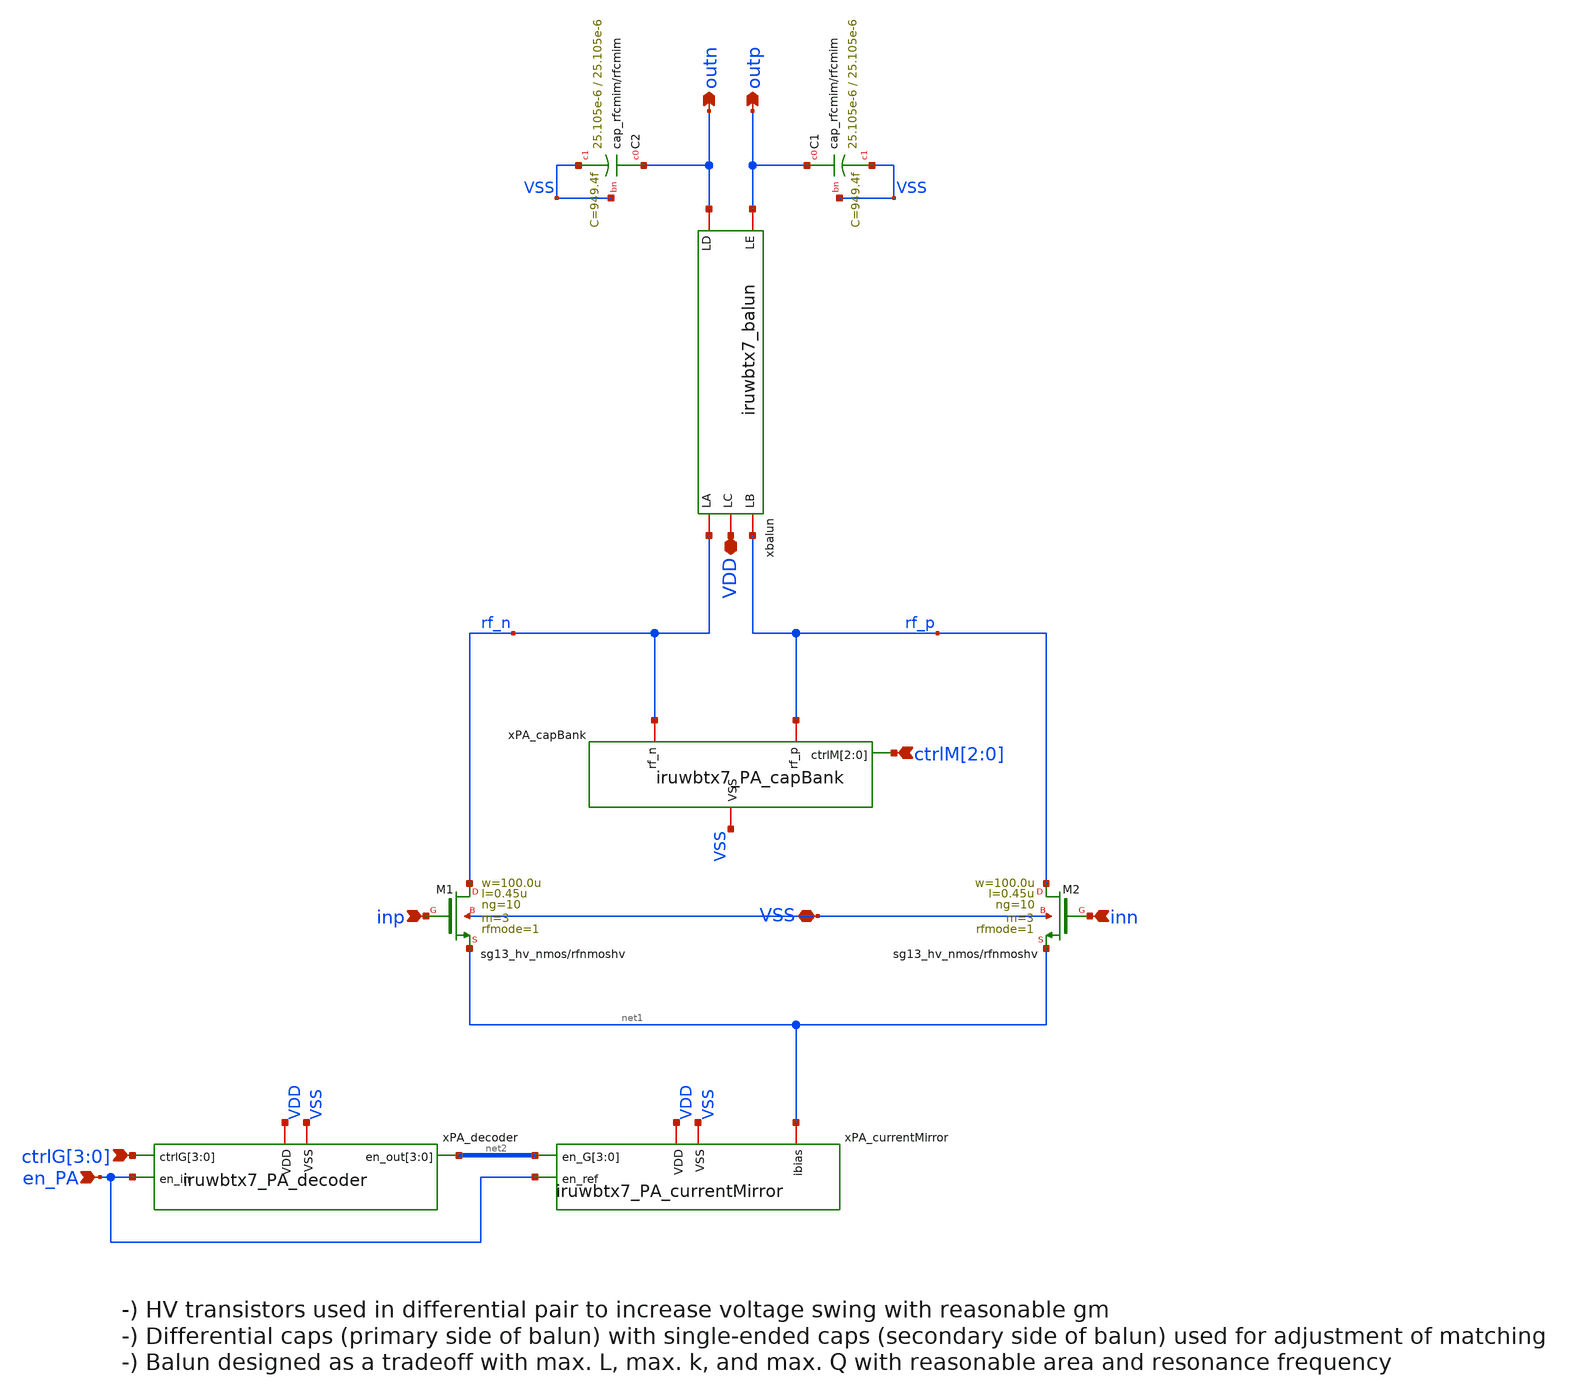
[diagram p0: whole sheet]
** sch_path: xschem/iruwbtx7_PA.sch
* IHP-GmbH/IHP-Open-PDK/ihp-sg13g2/libs.tech/xschem/sg13g2_stdcells/sg13g2_inv_16.sch:
* Copyright 2023 IHP PDK Authors
* Licensed under the Apache License, Version 2.0 (the "License");
**.subckt iruwbtx7_PA VDD outn outp ctrlM[2],ctrlM[1],ctrlM[0] inp inn VSS
*+ ctrlG[3],ctrlG[2],ctrlG[1],ctrlG[0] en_PA
*.iopin VDD
*.opin outn
*.opin outp
*.ipin ctrlM[2],ctrlM[1],ctrlM[0]
*.ipin inp
*.ipin inn
*.iopin VSS
*.ipin ctrlG[3],ctrlG[2],ctrlG[1],ctrlG[0]
*.ipin en_PA
xbalun outn outp VDD rf_p rf_n iruwbtx7_balun
XC2 outn VSS VSS cap_rfcmim w=25.105e-6 l=25.105e-6 wfeed=3.0e-6 m=1 mm_ok=1
XC1 outp VSS VSS cap_rfcmim w=25.105e-6 l=25.105e-6 wfeed=3.0e-6 m=1 mm_ok=1
xPA_capBank rf_n rf_p ctrlM[2] ctrlM[1] ctrlM[0] VSS iruwbtx7_PA_capBank
XM2 rf_p inn net1 VSS sg13_hv_nmos w=100.0u l=0.45u ng=10 m=3 rfmode=1 mm_ok=1
XM1 rf_n inp net1 VSS sg13_hv_nmos w=100.0u l=0.45u ng=10 m=3 rfmode=1 mm_ok=1
xPA_currentMirror VDD net2[3] net2[2] net2[1] net2[0] net1 en_PA VSS iruwbtx7_PA_currentMirror
xPA_decoder VDD VSS ctrlG[3] ctrlG[2] ctrlG[1] ctrlG[0] net2[3] net2[2] net2[1] net2[0] en_PA
+ iruwbtx7_PA_decoder
**.ends

* expanding   symbol:  iruwbtx7_balun.sym # of pins=5
** sym_path: xschem/iruwbtx7_balun.sym
** sch_path: xschem/iruwbtx7_balun.sch
.subckt iruwbtx7_balun LD LE LC LB LA
*.iopin LC
*.iopin LA
*.iopin LB
*.iopin LD
*.iopin LE
L1 LC net2 411p m=1
L2 net1 LC 411p m=1
R1 net2 LA 2.18 m=1
R2 LB net1 2.18 m=1
L3 net3 net5 483p m=1
L4 net4 net3 483p m=1
R3 net5 LD 3.6 m=1
R4 LE net4 3.6 m=1
K1 L1 L3 0.74
K2 L2 L4 0.74
.ends


* expanding   symbol:  iruwbtx7_PA_capBank.sym # of pins=4
** sym_path: xschem/iruwbtx7_PA_capBank.sym
** sch_path: xschem/iruwbtx7_PA_capBank.sch
.subckt iruwbtx7_PA_capBank rf_n rf_p ctrlM[2] ctrlM[1] ctrlM[0] VSS
*.ipin ctrlM[2],ctrlM[1],ctrlM[0]
*.iopin VSS
*.iopin rf_p
*.iopin rf_n
XC5[3] rf_n net1 VSS cap_rfcmim w=7.0e-6 l=7.0e-6 wfeed=1.0e-6 m=1 mm_ok=1
XC5[2] rf_n net1 VSS cap_rfcmim w=7.0e-6 l=7.0e-6 wfeed=1.0e-6 m=1 mm_ok=1
XC5[1] rf_n net1 VSS cap_rfcmim w=7.0e-6 l=7.0e-6 wfeed=1.0e-6 m=1 mm_ok=1
XC5[0] rf_n net1 VSS cap_rfcmim w=7.0e-6 l=7.0e-6 wfeed=1.0e-6 m=1 mm_ok=1
XM7 net1 ctrlM[2] VSS VSS sg13_lv_nmos w=10.0u l=0.13u ng=1 m=4 rfmode=1 mm_ok=1
XM8 net2 ctrlM[2] VSS VSS sg13_lv_nmos w=10.0u l=0.13u ng=1 m=4 rfmode=1 mm_ok=1
XM9 net1 ctrlM[2] net2 VSS sg13_lv_nmos w=10.0u l=0.13u ng=1 m=8 rfmode=1 mm_ok=1
XC6[3] rf_p net2 VSS cap_rfcmim w=7.0e-6 l=7.0e-6 wfeed=1.0e-6 m=1 mm_ok=1
XC6[2] rf_p net2 VSS cap_rfcmim w=7.0e-6 l=7.0e-6 wfeed=1.0e-6 m=1 mm_ok=1
XC6[1] rf_p net2 VSS cap_rfcmim w=7.0e-6 l=7.0e-6 wfeed=1.0e-6 m=1 mm_ok=1
XC6[0] rf_p net2 VSS cap_rfcmim w=7.0e-6 l=7.0e-6 wfeed=1.0e-6 m=1 mm_ok=1
XC7[1] rf_n net3 VSS cap_rfcmim w=7.0e-6 l=7.0e-6 wfeed=1.0e-6 m=1 mm_ok=1
XC7[0] rf_n net3 VSS cap_rfcmim w=7.0e-6 l=7.0e-6 wfeed=1.0e-6 m=1 mm_ok=1
XM10 net3 ctrlM[1] VSS VSS sg13_lv_nmos w=10.0u l=0.13u ng=1 m=2 rfmode=1 mm_ok=1
XM11 net4 ctrlM[1] VSS VSS sg13_lv_nmos w=10.0u l=0.13u ng=1 m=2 rfmode=1 mm_ok=1
XM12 net3 ctrlM[1] net4 VSS sg13_lv_nmos w=10.0u l=0.13u ng=1 m=4 rfmode=1 mm_ok=1
XC8[1] rf_p net4 VSS cap_rfcmim w=7.0e-6 l=7.0e-6 wfeed=1.0e-6 m=1 mm_ok=1
XC8[0] rf_p net4 VSS cap_rfcmim w=7.0e-6 l=7.0e-6 wfeed=1.0e-6 m=1 mm_ok=1
XC9 rf_n net5 VSS cap_rfcmim w=7.0e-6 l=7.0e-6 wfeed=1.0e-6 m=1 mm_ok=1
XM13 net5 ctrlM[0] VSS VSS sg13_lv_nmos w=10.0u l=0.13u ng=1 m=1 rfmode=1 mm_ok=1
XM14 net6 ctrlM[0] VSS VSS sg13_lv_nmos w=10.0u l=0.13u ng=1 m=1 rfmode=1 mm_ok=1
XM15 net5 ctrlM[0] net6 VSS sg13_lv_nmos w=10.0u l=0.13u ng=1 m=2 rfmode=1 mm_ok=1
XC10 rf_p net6 VSS cap_rfcmim w=7.0e-6 l=7.0e-6 wfeed=1.0e-6 m=1 mm_ok=1
.ends


* expanding   symbol:  iruwbtx7_PA_currentMirror.sym # of pins=5
** sym_path: xschem/iruwbtx7_PA_currentMirror.sym
** sch_path: xschem/iruwbtx7_PA_currentMirror.sch
.subckt iruwbtx7_PA_currentMirror VDD en_G[3] en_G[2] en_G[1] en_G[0] ibias en_ref VSS
*.iopin ibias
*.ipin en_ref
*.iopin VSS
*.iopin VDD
*.ipin en_G[3],en_G[2],en_G[1],en_G[0]
XM1 ibias net2 net1 VSS sg13_lv_nmos w=80.0u l=0.5u ng=10 m=2 mm_ok=1
XM2 net1 en_G[0] VSS VSS sg13_lv_nmos w=30.0u l=0.13u ng=10 m=2 mm_ok=1
XM3 ibias net2 net3 VSS sg13_lv_nmos w=80.0u l=0.5u ng=10 m=4 mm_ok=1
XM4 net3 en_G[1] VSS VSS sg13_lv_nmos w=30.0u l=0.13u ng=10 m=4 mm_ok=1
XM5 ibias net2 net4 VSS sg13_lv_nmos w=80.0u l=0.5u ng=10 m=8 mm_ok=1
XM6 net4 en_G[2] VSS VSS sg13_lv_nmos w=30.0u l=0.13u ng=10 m=8 mm_ok=1
XM7 ibias net2 net5 VSS sg13_lv_nmos w=80.0u l=0.5u ng=10 m=16 mm_ok=1
XM8 net5 en_G[3] VSS VSS sg13_lv_nmos w=30.0u l=0.13u ng=10 m=16 mm_ok=1
XM9 net2 net2 net6 VSS sg13_lv_nmos w=80.0u l=0.5u ng=10 m=1 mm_ok=1
XM10 net6 en_ref VSS VSS sg13_lv_nmos w=30.0u l=0.13u ng=10 m=1 mm_ok=1
XR1 VDD net2 VSS rppd w=1.7e-6 l=6.3e-6 m=1 b=0 mm_ok=1
.ends


* expanding   symbol:  iruwbtx7_PA_decoder.sym # of pins=5
** sym_path: xschem/iruwbtx7_PA_decoder.sym
** sch_path: xschem/iruwbtx7_PA_decoder.sch
.subckt iruwbtx7_PA_decoder VDD VSS ctrlG[3] ctrlG[2] ctrlG[1] ctrlG[0] en_out[3] en_out[2]
+ en_out[1] en_out[0] en_in
*.ipin ctrlG[3],ctrlG[2],ctrlG[1],ctrlG[0]
*.ipin en_in
*.opin en_out[3],en_out[2],en_out[1],en_out[0]
*.iopin VDD
*.iopin VSS
x10[3] net3[3] ctrlG[3] en_in VDD VSS sg13g2_nand2_2
x10[2] net3[2] ctrlG[2] en_in VDD VSS sg13g2_nand2_2
x10[1] net3[1] ctrlG[1] en_in VDD VSS sg13g2_nand2_2
x10[0] net3[0] ctrlG[0] en_in VDD VSS sg13g2_nand2_2
x9[3] net1[3] net3[3] VDD VSS sg13g2_inv_2
x9[2] net1[2] net3[2] VDD VSS sg13g2_inv_2
x9[1] net1[1] net3[1] VDD VSS sg13g2_inv_2
x9[0] net1[0] net3[0] VDD VSS sg13g2_inv_2
x1[3] net2[3] net1[3] VDD VSS sg13g2_inv_8
x1[2] net2[2] net1[2] VDD VSS sg13g2_inv_8
x1[1] net2[1] net1[1] VDD VSS sg13g2_inv_8
x1[0] net2[0] net1[0] VDD VSS sg13g2_inv_8
x11[3] en_out[3] net2[3] VDD VSS sg13g2_inv_16
x11[2] en_out[2] net2[2] VDD VSS sg13g2_inv_16
x11[1] en_out[1] net2[1] VDD VSS sg13g2_inv_16
x11[0] en_out[0] net2[0] VDD VSS sg13g2_inv_16
.ends


* expanding   symbol:  sg13g2_nand2_2.sym # of pins=3
** sym_path: sg13g2_nand2_2.sym
** sch_path: sg13g2_nand2_2.sch
.subckt sg13g2_nand2_2 Y A B VDD VSS
*.iopin VDD
*.iopin VSS
*.opin Y
*.ipin B
*.ipin A
XM1 Y A net1 VSS sg13_lv_nmos w=1.44u l=130.00n ng=2 m=1 mm_ok=1
XM2 net1 B VSS VSS sg13_lv_nmos w=1.44u l=130.00n ng=2 m=1 mm_ok=1
XM3 Y A VDD VDD sg13_lv_pmos w=2.24u l=130.00n ng=2 m=1 mm_ok=1
XM4 Y B VDD VDD sg13_lv_pmos w=2.24u l=130.00n ng=2 m=1 mm_ok=1
.ends


* expanding   symbol:  sg13g2_inv_2.sym # of pins=2
** sym_path: sg13g2_inv_2.sym
** sch_path: sg13g2_inv_2.sch
.subckt sg13g2_inv_2 Y A VDD VSS
*.opin Y
*.ipin A
*.iopin VDD
*.iopin VSS
XM1 Y A VSS VSS sg13_lv_nmos w=1.48u l=130.00n ng=2 m=1 mm_ok=1
XM2 Y A VDD VDD sg13_lv_pmos w=2.24u l=130.00n ng=2 m=1 mm_ok=1
.ends


* expanding   symbol:  sg13g2_inv_8.sym # of pins=2
** sym_path: sg13g2_inv_8.sym
** sch_path: sg13g2_inv_8.sch
.subckt sg13g2_inv_8 Y A VDD VSS
*.opin Y
*.ipin A
*.iopin VDD
*.iopin VSS
XM1 Y A VSS VSS sg13_lv_nmos w=5.92u l=130.00n ng=8 m=1 mm_ok=1
XM2 Y A VDD VDD sg13_lv_pmos w=8.96u l=130.00n ng=8 m=1 mm_ok=1
.ends


* expanding   symbol:  sg13g2_inv_16.sym # of pins=2
** sym_path: sg13g2_inv_16.sym
** sch_path: sg13g2_inv_16.sch
.subckt sg13g2_inv_16 Y A VDD VSS
*.opin Y
*.iopin VSS
*.ipin A
*.iopin VDD
XM1 Y A VSS VSS sg13_lv_nmos w=11.84u l=130.00n ng=16 m=1 mm_ok=1
XM2 Y A VDD VDD sg13_lv_pmos w=17.92u l=130.00n ng=16 m=1 mm_ok=1
.ends

.end
